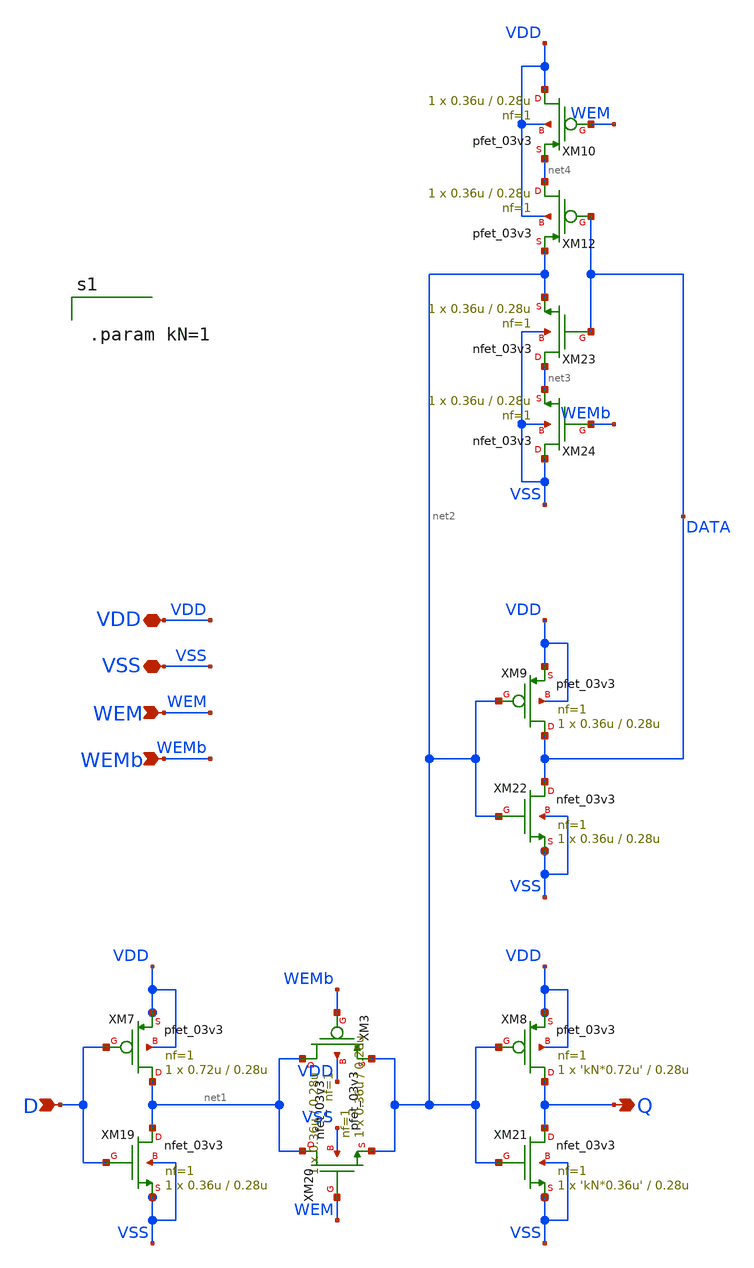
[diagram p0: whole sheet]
** sch_path: CAD3/master_latch.sch
**.subckt master_latch D WEMb WEM VSS VDD Q
*.ipin D
*.ipin WEMb
*.ipin WEM
*.iopin VSS
*.iopin VDD
*.opin Q
XM3 net1 WEMb net2 VDD pfet_03v3 L=0.28u W=0.36u nf=1 ad='int((nf+1)/2) * W/nf * 0.18u' as='int((nf+2)/2) * W/nf * 0.18u'
+ pd='2*int((nf+1)/2) * (W/nf + 0.18u)' ps='2*int((nf+2)/2) * (W/nf + 0.18u)' nrd='0.18u / W' nrs='0.18u / W'
+ sa=0 sb=0 sd=0 m=1
XM7 net1 D VDD VDD pfet_03v3 L=0.28u W=0.72u nf=1 ad='int((nf+1)/2) * W/nf * 0.18u' as='int((nf+2)/2) * W/nf * 0.18u'
+ pd='2*int((nf+1)/2) * (W/nf + 0.18u)' ps='2*int((nf+2)/2) * (W/nf + 0.18u)' nrd='0.18u / W' nrs='0.18u / W'
+ sa=0 sb=0 sd=0 m=1
XM8 Q net2 VDD VDD pfet_03v3 L=0.28u W='kN*0.72u' nf=1 ad='int((nf+1)/2) * W/nf * 0.18u' as='int((nf+2)/2) * W/nf * 0.18u'
+ pd='2*int((nf+1)/2) * (W/nf + 0.18u)' ps='2*int((nf+2)/2) * (W/nf + 0.18u)' nrd='0.18u / W' nrs='0.18u / W'
+ sa=0 sb=0 sd=0 m=1
XM9 DATA net2 VDD VDD pfet_03v3 L=0.28u W=0.36u nf=1 ad='int((nf+1)/2) * W/nf * 0.18u' as='int((nf+2)/2) * W/nf * 0.18u'
+ pd='2*int((nf+1)/2) * (W/nf + 0.18u)' ps='2*int((nf+2)/2) * (W/nf + 0.18u)' nrd='0.18u / W' nrs='0.18u / W'
+ sa=0 sb=0 sd=0 m=1
XM10 VDD WEM net4 VDD pfet_03v3 L=0.28u W=0.36u nf=1 ad='int((nf+1)/2) * W/nf * 0.18u' as='int((nf+2)/2) * W/nf * 0.18u'
+ pd='2*int((nf+1)/2) * (W/nf + 0.18u)' ps='2*int((nf+2)/2) * (W/nf + 0.18u)' nrd='0.18u / W' nrs='0.18u / W'
+ sa=0 sb=0 sd=0 m=1
XM12 net4 DATA net2 VDD pfet_03v3 L=0.28u W=0.36u nf=1 ad='int((nf+1)/2) * W/nf * 0.18u' as='int((nf+2)/2) * W/nf * 0.18u'
+ pd='2*int((nf+1)/2) * (W/nf + 0.18u)' ps='2*int((nf+2)/2) * (W/nf + 0.18u)' nrd='0.18u / W' nrs='0.18u / W'
+ sa=0 sb=0 sd=0 m=1
XM19 net1 D VSS VSS nfet_03v3 L=0.28u W=0.36u nf=1 ad='int((nf+1)/2) * W/nf * 0.18u' as='int((nf+2)/2) * W/nf * 0.18u'
+ pd='2*int((nf+1)/2) * (W/nf + 0.18u)' ps='2*int((nf+2)/2) * (W/nf + 0.18u)' nrd='0.18u / W' nrs='0.18u / W'
+ sa=0 sb=0 sd=0 m=1
XM20 net1 WEM net2 VSS nfet_03v3 L=0.28u W=0.36u nf=1 ad='int((nf+1)/2) * W/nf * 0.18u' as='int((nf+2)/2) * W/nf * 0.18u'
+ pd='2*int((nf+1)/2) * (W/nf + 0.18u)' ps='2*int((nf+2)/2) * (W/nf + 0.18u)' nrd='0.18u / W' nrs='0.18u / W'
+ sa=0 sb=0 sd=0 m=1
XM21 Q net2 VSS VSS nfet_03v3 L=0.28u W='kN*0.36u' nf=1 ad='int((nf+1)/2) * W/nf * 0.18u' as='int((nf+2)/2) * W/nf * 0.18u'
+ pd='2*int((nf+1)/2) * (W/nf + 0.18u)' ps='2*int((nf+2)/2) * (W/nf + 0.18u)' nrd='0.18u / W' nrs='0.18u / W'
+ sa=0 sb=0 sd=0 m=1
XM22 DATA net2 VSS VSS nfet_03v3 L=0.28u W=0.36u nf=1 ad='int((nf+1)/2) * W/nf * 0.18u' as='int((nf+2)/2) * W/nf * 0.18u'
+ pd='2*int((nf+1)/2) * (W/nf + 0.18u)' ps='2*int((nf+2)/2) * (W/nf + 0.18u)' nrd='0.18u / W' nrs='0.18u / W'
+ sa=0 sb=0 sd=0 m=1
XM23 net3 DATA net2 VSS nfet_03v3 L=0.28u W=0.36u nf=1 ad='int((nf+1)/2) * W/nf * 0.18u' as='int((nf+2)/2) * W/nf * 0.18u'
+ pd='2*int((nf+1)/2) * (W/nf + 0.18u)' ps='2*int((nf+2)/2) * (W/nf + 0.18u)' nrd='0.18u / W' nrs='0.18u / W'
+ sa=0 sb=0 sd=0 m=1
XM24 VSS WEMb net3 VSS nfet_03v3 L=0.28u W=0.36u nf=1 ad='int((nf+1)/2) * W/nf * 0.18u' as='int((nf+2)/2) * W/nf * 0.18u'
+ pd='2*int((nf+1)/2) * (W/nf + 0.18u)' ps='2*int((nf+2)/2) * (W/nf + 0.18u)' nrd='0.18u / W' nrs='0.18u / W'
+ sa=0 sb=0 sd=0 m=1
**** begin user architecture code


.param kN=1


**** end user architecture code
**.ends
.end
